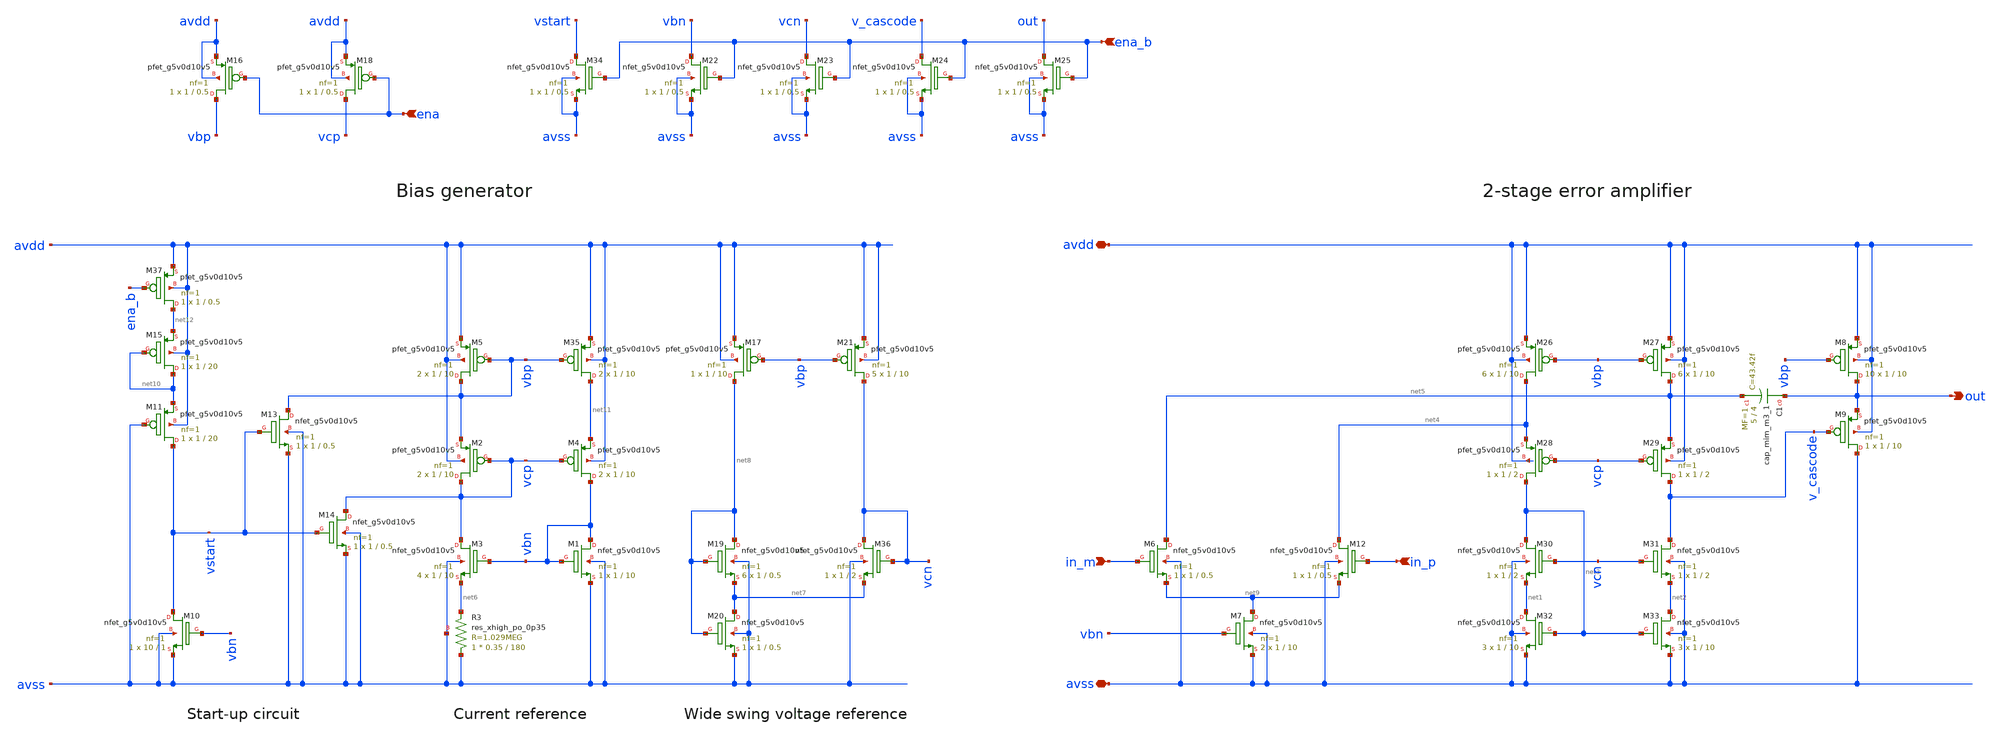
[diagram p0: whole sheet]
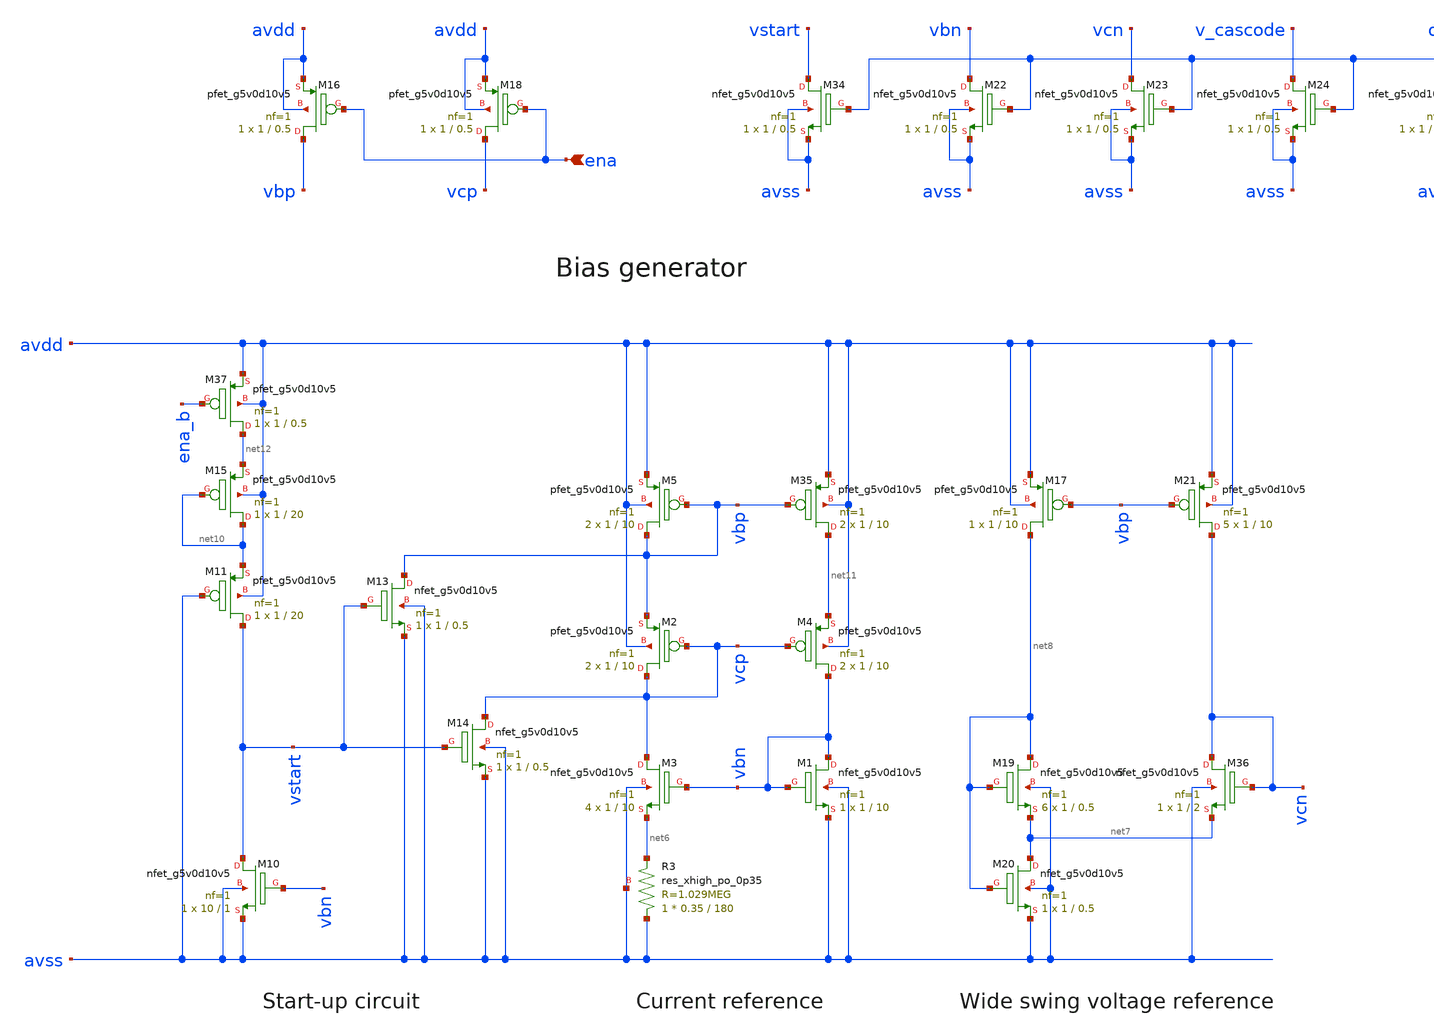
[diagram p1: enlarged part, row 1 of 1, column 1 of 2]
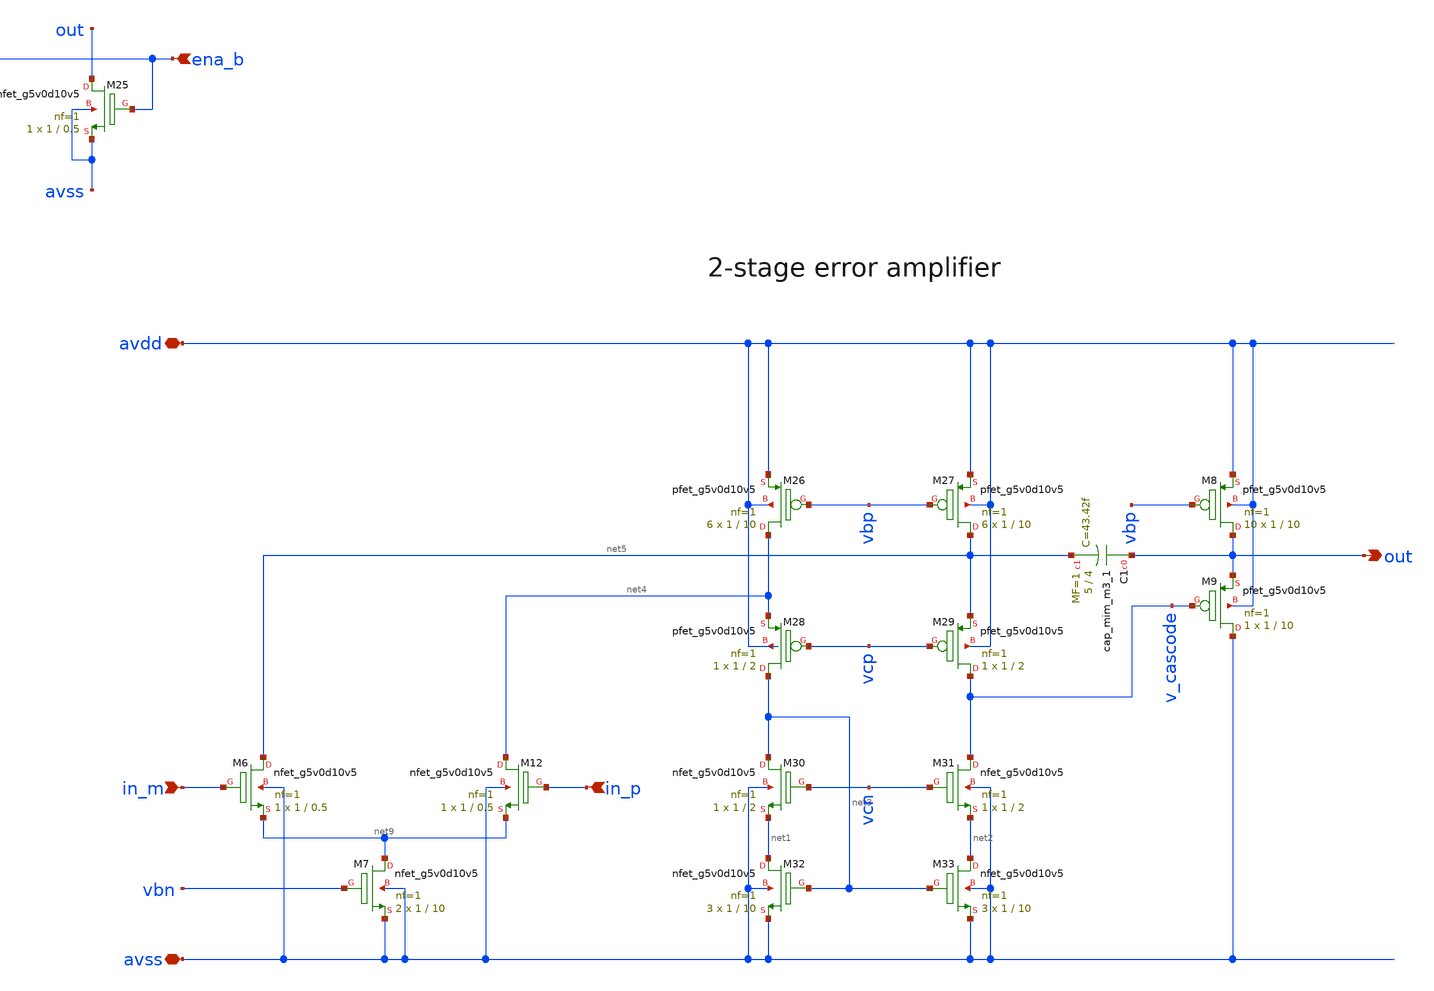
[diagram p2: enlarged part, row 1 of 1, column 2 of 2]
** sch_path: xschem/error_amplifier.sch
**.subckt error_amplifier avdd avss in_m in_p out ena ena_b
*.iopin avdd
*.iopin avss
*.ipin in_m
*.ipin in_p
*.opin out
*.ipin ena
*.ipin ena_b
XM1 vbn vbn avss avss sky130_fd_pr__nfet_g5v0d10v5 L=10 W=1 nf=1 ad='int((nf+1)/2) * W/nf * 0.29' as='int((nf+2)/2) * W/nf * 0.29'
+ pd='2*int((nf+1)/2) * (W/nf + 0.29)' ps='2*int((nf+2)/2) * (W/nf + 0.29)' nrd='0.29 / W' nrs='0.29 / W'
+ sa=0 sb=0 sd=0 mult=1 m=1
XM3 vcp vbn net6 avss sky130_fd_pr__nfet_g5v0d10v5 L=10 W=1 nf=1 ad='int((nf+1)/2) * W/nf * 0.29' as='int((nf+2)/2) * W/nf * 0.29'
+ pd='2*int((nf+1)/2) * (W/nf + 0.29)' ps='2*int((nf+2)/2) * (W/nf + 0.29)' nrd='0.29 / W' nrs='0.29 / W'
+ sa=0 sb=0 sd=0 mult=4 m=4
XM5 vbp vbp avdd avdd sky130_fd_pr__pfet_g5v0d10v5 L=10 W=1 nf=1 ad='int((nf+1)/2) * W/nf * 0.29' as='int((nf+2)/2) * W/nf * 0.29'
+ pd='2*int((nf+1)/2) * (W/nf + 0.29)' ps='2*int((nf+2)/2) * (W/nf + 0.29)' nrd='0.29 / W' nrs='0.29 / W'
+ sa=0 sb=0 sd=0 mult=2 m=2
XM26 net4 vbp avdd avdd sky130_fd_pr__pfet_g5v0d10v5 L=10 W=1 nf=1 ad='int((nf+1)/2) * W/nf * 0.29' as='int((nf+2)/2) * W/nf * 0.29'
+ pd='2*int((nf+1)/2) * (W/nf + 0.29)' ps='2*int((nf+2)/2) * (W/nf + 0.29)' nrd='0.29 / W' nrs='0.29 / W'
+ sa=0 sb=0 sd=0 mult=6 m=6
XM27 net5 vbp avdd avdd sky130_fd_pr__pfet_g5v0d10v5 L=10 W=1 nf=1 ad='int((nf+1)/2) * W/nf * 0.29' as='int((nf+2)/2) * W/nf * 0.29'
+ pd='2*int((nf+1)/2) * (W/nf + 0.29)' ps='2*int((nf+2)/2) * (W/nf + 0.29)' nrd='0.29 / W' nrs='0.29 / W'
+ sa=0 sb=0 sd=0 mult=6 m=6
XM28 net3 vcp net4 avdd sky130_fd_pr__pfet_g5v0d10v5 L=2 W=1 nf=1 ad='int((nf+1)/2) * W/nf * 0.29' as='int((nf+2)/2) * W/nf * 0.29'
+ pd='2*int((nf+1)/2) * (W/nf + 0.29)' ps='2*int((nf+2)/2) * (W/nf + 0.29)' nrd='0.29 / W' nrs='0.29 / W'
+ sa=0 sb=0 sd=0 mult=1 m=1
XM29 v_cascode vcp net5 avdd sky130_fd_pr__pfet_g5v0d10v5 L=2 W=1 nf=1 ad='int((nf+1)/2) * W/nf * 0.29'
+ as='int((nf+2)/2) * W/nf * 0.29' pd='2*int((nf+1)/2) * (W/nf + 0.29)' ps='2*int((nf+2)/2) * (W/nf + 0.29)'
+ nrd='0.29 / W' nrs='0.29 / W' sa=0 sb=0 sd=0 mult=1 m=1
XM30 net3 vcn net1 avss sky130_fd_pr__nfet_g5v0d10v5 L=2 W=1 nf=1 ad='int((nf+1)/2) * W/nf * 0.29' as='int((nf+2)/2) * W/nf * 0.29'
+ pd='2*int((nf+1)/2) * (W/nf + 0.29)' ps='2*int((nf+2)/2) * (W/nf + 0.29)' nrd='0.29 / W' nrs='0.29 / W'
+ sa=0 sb=0 sd=0 mult=1 m=1
XM31 v_cascode vcn net2 avss sky130_fd_pr__nfet_g5v0d10v5 L=2 W=1 nf=1 ad='int((nf+1)/2) * W/nf * 0.29'
+ as='int((nf+2)/2) * W/nf * 0.29' pd='2*int((nf+1)/2) * (W/nf + 0.29)' ps='2*int((nf+2)/2) * (W/nf + 0.29)'
+ nrd='0.29 / W' nrs='0.29 / W' sa=0 sb=0 sd=0 mult=1 m=1
XM32 net1 net3 avss avss sky130_fd_pr__nfet_g5v0d10v5 L=10 W=1 nf=1 ad='int((nf+1)/2) * W/nf * 0.29'
+ as='int((nf+2)/2) * W/nf * 0.29' pd='2*int((nf+1)/2) * (W/nf + 0.29)' ps='2*int((nf+2)/2) * (W/nf + 0.29)'
+ nrd='0.29 / W' nrs='0.29 / W' sa=0 sb=0 sd=0 mult=3 m=3
XM33 net2 net3 avss avss sky130_fd_pr__nfet_g5v0d10v5 L=10 W=1 nf=1 ad='int((nf+1)/2) * W/nf * 0.29'
+ as='int((nf+2)/2) * W/nf * 0.29' pd='2*int((nf+1)/2) * (W/nf + 0.29)' ps='2*int((nf+2)/2) * (W/nf + 0.29)'
+ nrd='0.29 / W' nrs='0.29 / W' sa=0 sb=0 sd=0 mult=3 m=3
XM35 net11 vbp avdd avdd sky130_fd_pr__pfet_g5v0d10v5 L=10 W=1 nf=1 ad='int((nf+1)/2) * W/nf * 0.29'
+ as='int((nf+2)/2) * W/nf * 0.29' pd='2*int((nf+1)/2) * (W/nf + 0.29)' ps='2*int((nf+2)/2) * (W/nf + 0.29)'
+ nrd='0.29 / W' nrs='0.29 / W' sa=0 sb=0 sd=0 mult=2 m=2
XR3 avss net6 avss sky130_fd_pr__res_xhigh_po_0p35 L=180 mult=1 m=1
XM9 avss v_cascode out avdd sky130_fd_pr__pfet_g5v0d10v5 L=10 W=1 nf=1 ad='int((nf+1)/2) * W/nf * 0.29'
+ as='int((nf+2)/2) * W/nf * 0.29' pd='2*int((nf+1)/2) * (W/nf + 0.29)' ps='2*int((nf+2)/2) * (W/nf + 0.29)'
+ nrd='0.29 / W' nrs='0.29 / W' sa=0 sb=0 sd=0 mult=1 m=1
XM8 out vbp avdd avdd sky130_fd_pr__pfet_g5v0d10v5 L=10 W=1 nf=1 ad='int((nf+1)/2) * W/nf * 0.29' as='int((nf+2)/2) * W/nf * 0.29'
+ pd='2*int((nf+1)/2) * (W/nf + 0.29)' ps='2*int((nf+2)/2) * (W/nf + 0.29)' nrd='0.29 / W' nrs='0.29 / W'
+ sa=0 sb=0 sd=0 mult=10 m=10
XM17 net8 vbp avdd avdd sky130_fd_pr__pfet_g5v0d10v5 L=10 W=1 nf=1 ad='int((nf+1)/2) * W/nf * 0.29' as='int((nf+2)/2) * W/nf * 0.29'
+ pd='2*int((nf+1)/2) * (W/nf + 0.29)' ps='2*int((nf+2)/2) * (W/nf + 0.29)' nrd='0.29 / W' nrs='0.29 / W'
+ sa=0 sb=0 sd=0 mult=1 m=1
XM19 net8 net8 net7 avss sky130_fd_pr__nfet_g5v0d10v5 L=0.5 W=1 nf=1 ad='int((nf+1)/2) * W/nf * 0.29'
+ as='int((nf+2)/2) * W/nf * 0.29' pd='2*int((nf+1)/2) * (W/nf + 0.29)' ps='2*int((nf+2)/2) * (W/nf + 0.29)'
+ nrd='0.29 / W' nrs='0.29 / W' sa=0 sb=0 sd=0 mult=6 m=6
XM20 net7 net8 avss avss sky130_fd_pr__nfet_g5v0d10v5 L=0.5 W=1 nf=1 ad='int((nf+1)/2) * W/nf * 0.29'
+ as='int((nf+2)/2) * W/nf * 0.29' pd='2*int((nf+1)/2) * (W/nf + 0.29)' ps='2*int((nf+2)/2) * (W/nf + 0.29)'
+ nrd='0.29 / W' nrs='0.29 / W' sa=0 sb=0 sd=0 mult=1 m=1
XM21 vcn vbp avdd avdd sky130_fd_pr__pfet_g5v0d10v5 L=10 W=1 nf=1 ad='int((nf+1)/2) * W/nf * 0.29' as='int((nf+2)/2) * W/nf * 0.29'
+ pd='2*int((nf+1)/2) * (W/nf + 0.29)' ps='2*int((nf+2)/2) * (W/nf + 0.29)' nrd='0.29 / W' nrs='0.29 / W'
+ sa=0 sb=0 sd=0 mult=5 m=5
XM36 vcn vcn net7 avss sky130_fd_pr__nfet_g5v0d10v5 L=2 W=1 nf=1 ad='int((nf+1)/2) * W/nf * 0.29' as='int((nf+2)/2) * W/nf * 0.29'
+ pd='2*int((nf+1)/2) * (W/nf + 0.29)' ps='2*int((nf+2)/2) * (W/nf + 0.29)' nrd='0.29 / W' nrs='0.29 / W'
+ sa=0 sb=0 sd=0 mult=1 m=1
XM6 net5 in_m net9 avss sky130_fd_pr__nfet_g5v0d10v5 L=0.5 W=1 nf=1 ad='int((nf+1)/2) * W/nf * 0.29'
+ as='int((nf+2)/2) * W/nf * 0.29' pd='2*int((nf+1)/2) * (W/nf + 0.29)' ps='2*int((nf+2)/2) * (W/nf + 0.29)'
+ nrd='0.29 / W' nrs='0.29 / W' sa=0 sb=0 sd=0 mult=1 m=1
XM7 net9 vbn avss avss sky130_fd_pr__nfet_g5v0d10v5 L=10 W=1 nf=1 ad='int((nf+1)/2) * W/nf * 0.29' as='int((nf+2)/2) * W/nf * 0.29'
+ pd='2*int((nf+1)/2) * (W/nf + 0.29)' ps='2*int((nf+2)/2) * (W/nf + 0.29)' nrd='0.29 / W' nrs='0.29 / W'
+ sa=0 sb=0 sd=0 mult=2 m=2
XM12 net4 in_p net9 avss sky130_fd_pr__nfet_g5v0d10v5 L=0.5 W=1 nf=1 ad='int((nf+1)/2) * W/nf * 0.29'
+ as='int((nf+2)/2) * W/nf * 0.29' pd='2*int((nf+1)/2) * (W/nf + 0.29)' ps='2*int((nf+2)/2) * (W/nf + 0.29)'
+ nrd='0.29 / W' nrs='0.29 / W' sa=0 sb=0 sd=0 mult=1 m=1
XM10 vstart vbn avss avss sky130_fd_pr__nfet_g5v0d10v5 L=1 W=10 nf=1 ad='int((nf+1)/2) * W/nf * 0.29'
+ as='int((nf+2)/2) * W/nf * 0.29' pd='2*int((nf+1)/2) * (W/nf + 0.29)' ps='2*int((nf+2)/2) * (W/nf + 0.29)'
+ nrd='0.29 / W' nrs='0.29 / W' sa=0 sb=0 sd=0 mult=1 m=1
XM11 vstart avss net10 avdd sky130_fd_pr__pfet_g5v0d10v5 L=20 W=1 nf=1 ad='int((nf+1)/2) * W/nf * 0.29'
+ as='int((nf+2)/2) * W/nf * 0.29' pd='2*int((nf+1)/2) * (W/nf + 0.29)' ps='2*int((nf+2)/2) * (W/nf + 0.29)'
+ nrd='0.29 / W' nrs='0.29 / W' sa=0 sb=0 sd=0 mult=1 m=1
XM2 vcp vcp vbp avdd sky130_fd_pr__pfet_g5v0d10v5 L=10 W=1 nf=1 ad='int((nf+1)/2) * W/nf * 0.29' as='int((nf+2)/2) * W/nf * 0.29'
+ pd='2*int((nf+1)/2) * (W/nf + 0.29)' ps='2*int((nf+2)/2) * (W/nf + 0.29)' nrd='0.29 / W' nrs='0.29 / W'
+ sa=0 sb=0 sd=0 mult=2 m=2
XM4 vbn vcp net11 avdd sky130_fd_pr__pfet_g5v0d10v5 L=10 W=1 nf=1 ad='int((nf+1)/2) * W/nf * 0.29' as='int((nf+2)/2) * W/nf * 0.29'
+ pd='2*int((nf+1)/2) * (W/nf + 0.29)' ps='2*int((nf+2)/2) * (W/nf + 0.29)' nrd='0.29 / W' nrs='0.29 / W'
+ sa=0 sb=0 sd=0 mult=2 m=2
XM13 vbp vstart avss avss sky130_fd_pr__nfet_g5v0d10v5 L=0.5 W=1 nf=1 ad='int((nf+1)/2) * W/nf * 0.29'
+ as='int((nf+2)/2) * W/nf * 0.29' pd='2*int((nf+1)/2) * (W/nf + 0.29)' ps='2*int((nf+2)/2) * (W/nf + 0.29)'
+ nrd='0.29 / W' nrs='0.29 / W' sa=0 sb=0 sd=0 mult=1 m=1
XM14 vcp vstart avss avss sky130_fd_pr__nfet_g5v0d10v5 L=0.5 W=1 nf=1 ad='int((nf+1)/2) * W/nf * 0.29'
+ as='int((nf+2)/2) * W/nf * 0.29' pd='2*int((nf+1)/2) * (W/nf + 0.29)' ps='2*int((nf+2)/2) * (W/nf + 0.29)'
+ nrd='0.29 / W' nrs='0.29 / W' sa=0 sb=0 sd=0 mult=1 m=1
XM15 net10 net10 net12 avdd sky130_fd_pr__pfet_g5v0d10v5 L=20 W=1 nf=1 ad='int((nf+1)/2) * W/nf * 0.29'
+ as='int((nf+2)/2) * W/nf * 0.29' pd='2*int((nf+1)/2) * (W/nf + 0.29)' ps='2*int((nf+2)/2) * (W/nf + 0.29)'
+ nrd='0.29 / W' nrs='0.29 / W' sa=0 sb=0 sd=0 mult=1 m=1
XM16 vbp ena avdd avdd sky130_fd_pr__pfet_g5v0d10v5 L=0.5 W=1 nf=1 ad='int((nf+1)/2) * W/nf * 0.29' as='int((nf+2)/2) * W/nf * 0.29'
+ pd='2*int((nf+1)/2) * (W/nf + 0.29)' ps='2*int((nf+2)/2) * (W/nf + 0.29)' nrd='0.29 / W' nrs='0.29 / W'
+ sa=0 sb=0 sd=0 mult=1 m=1
XM18 vcp ena avdd avdd sky130_fd_pr__pfet_g5v0d10v5 L=0.5 W=1 nf=1 ad='int((nf+1)/2) * W/nf * 0.29' as='int((nf+2)/2) * W/nf * 0.29'
+ pd='2*int((nf+1)/2) * (W/nf + 0.29)' ps='2*int((nf+2)/2) * (W/nf + 0.29)' nrd='0.29 / W' nrs='0.29 / W'
+ sa=0 sb=0 sd=0 mult=1 m=1
XM22 vbn ena_b avss avss sky130_fd_pr__nfet_g5v0d10v5 L=0.5 W=1 nf=1 ad='int((nf+1)/2) * W/nf * 0.29'
+ as='int((nf+2)/2) * W/nf * 0.29' pd='2*int((nf+1)/2) * (W/nf + 0.29)' ps='2*int((nf+2)/2) * (W/nf + 0.29)'
+ nrd='0.29 / W' nrs='0.29 / W' sa=0 sb=0 sd=0 mult=1 m=1
XM23 vcn ena_b avss avss sky130_fd_pr__nfet_g5v0d10v5 L=0.5 W=1 nf=1 ad='int((nf+1)/2) * W/nf * 0.29'
+ as='int((nf+2)/2) * W/nf * 0.29' pd='2*int((nf+1)/2) * (W/nf + 0.29)' ps='2*int((nf+2)/2) * (W/nf + 0.29)'
+ nrd='0.29 / W' nrs='0.29 / W' sa=0 sb=0 sd=0 mult=1 m=1
XM24 v_cascode ena_b avss avss sky130_fd_pr__nfet_g5v0d10v5 L=0.5 W=1 nf=1 ad='int((nf+1)/2) * W/nf * 0.29'
+ as='int((nf+2)/2) * W/nf * 0.29' pd='2*int((nf+1)/2) * (W/nf + 0.29)' ps='2*int((nf+2)/2) * (W/nf + 0.29)'
+ nrd='0.29 / W' nrs='0.29 / W' sa=0 sb=0 sd=0 mult=1 m=1
XM25 out ena_b avss avss sky130_fd_pr__nfet_g5v0d10v5 L=0.5 W=1 nf=1 ad='int((nf+1)/2) * W/nf * 0.29'
+ as='int((nf+2)/2) * W/nf * 0.29' pd='2*int((nf+1)/2) * (W/nf + 0.29)' ps='2*int((nf+2)/2) * (W/nf + 0.29)'
+ nrd='0.29 / W' nrs='0.29 / W' sa=0 sb=0 sd=0 mult=1 m=1
XM34 vstart ena_b avss avss sky130_fd_pr__nfet_g5v0d10v5 L=0.5 W=1 nf=1 ad='int((nf+1)/2) * W/nf * 0.29'
+ as='int((nf+2)/2) * W/nf * 0.29' pd='2*int((nf+1)/2) * (W/nf + 0.29)' ps='2*int((nf+2)/2) * (W/nf + 0.29)'
+ nrd='0.29 / W' nrs='0.29 / W' sa=0 sb=0 sd=0 mult=1 m=1
XM37 net12 ena_b avdd avdd sky130_fd_pr__pfet_g5v0d10v5 L=0.5 W=1 nf=1 ad='int((nf+1)/2) * W/nf * 0.29'
+ as='int((nf+2)/2) * W/nf * 0.29' pd='2*int((nf+1)/2) * (W/nf + 0.29)' ps='2*int((nf+2)/2) * (W/nf + 0.29)'
+ nrd='0.29 / W' nrs='0.29 / W' sa=0 sb=0 sd=0 mult=1 m=1
XC1 out net5 sky130_fd_pr__cap_mim_m3_1 W=5 L=4 MF=1 m=1
**.ends
.end
